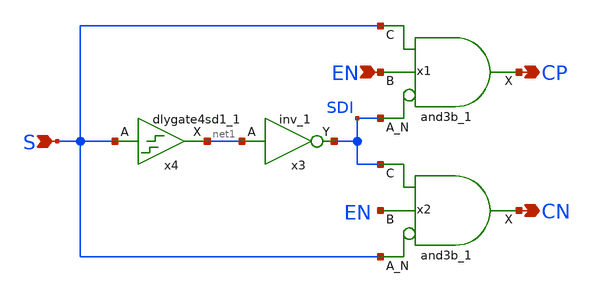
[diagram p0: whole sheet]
** sch_path: hvlsctrlgen.sch
**.subckt hvlsctrlgen S EN CP CN
*.ipin S
*.ipin EN
*.opin CP
*.opin CN
x1 SDI EN S VGND VNB VPB VPWR CP sky130_fd_sc_hd__and3b_1
x2 S EN SDI VGND VNB VPB VPWR CN sky130_fd_sc_hd__and3b_1
x3 net1 VGND VNB VPB VPWR SDI sky130_fd_sc_hd__inv_1
x4 S VGND VNB VPB VPWR net1 sky130_fd_sc_hd__dlygate4sd1_1
**.ends
.end
